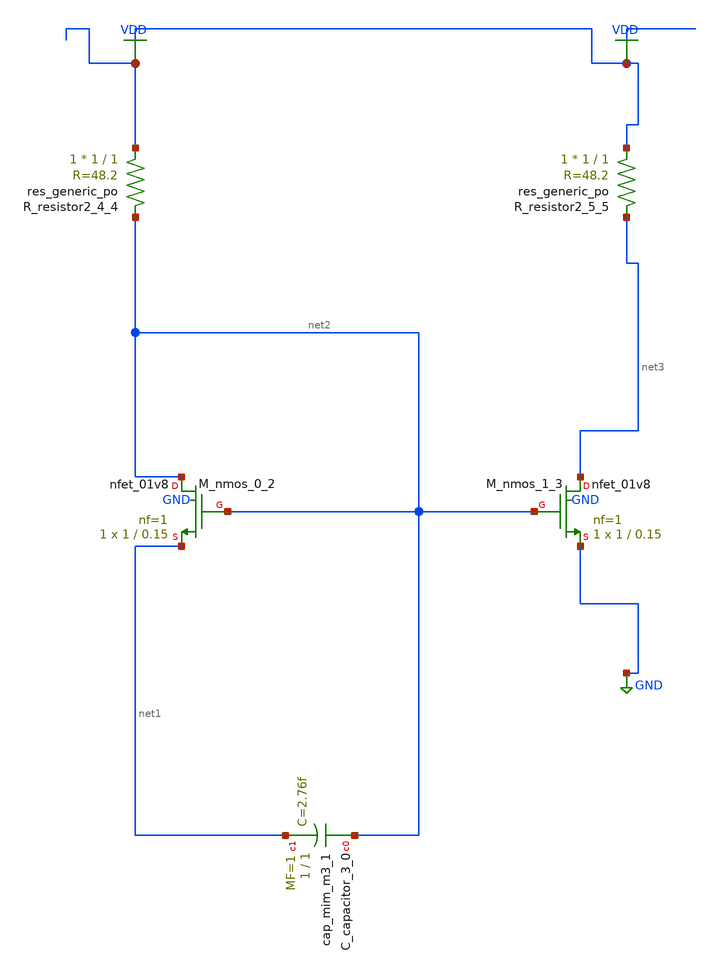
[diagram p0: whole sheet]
** sch_path: schematics/AMSNet/341.sch
**.subckt 341
XC_capacitor_3_0 net2 net1 sky130_fd_pr__cap_mim_m3_1 W=1 L=1 MF=1 m=1
XM_nmos_0_2 net2 net2 net1 GND sky130_fd_pr__nfet_01v8 L=0.15 W=1 nf=1 ad='int((1 + 1)/2) * 1 / 1 * 0.29'
+ as='int((1 + 2)/2) * 1 / 1 * 0.29' pd='2*int((1 + 1)/2) * (1 / 1 + 0.29)' ps='2*int((1 + 2)/2) * (1 / 1 + 0.29)'
+ nrd='0.29 / 1 ' nrs='0.29 / 1 ' sa=0 sb=0 sd=0 mult=1 m=1
XM_nmos_1_3 net3 net2 GND GND sky130_fd_pr__nfet_01v8 L=0.15 W=1 nf=1 ad='int((1 + 1)/2) * 1 / 1 * 0.29'
+ as='int((1 + 2)/2) * 1 / 1 * 0.29' pd='2*int((1 + 1)/2) * (1 / 1 + 0.29)' ps='2*int((1 + 2)/2) * (1 / 1 + 0.29)'
+ nrd='0.29 / 1 ' nrs='0.29 / 1 ' sa=0 sb=0 sd=0 mult=1 m=1
XR_resistor2_4_4 VDD net2 sky130_fd_pr__res_generic_po W=1 L=1 m=1
XR_resistor2_5_5 VDD net3 sky130_fd_pr__res_generic_po W=1 L=1 m=1
**.ends
.GLOBAL GND
.GLOBAL VDD
.end
